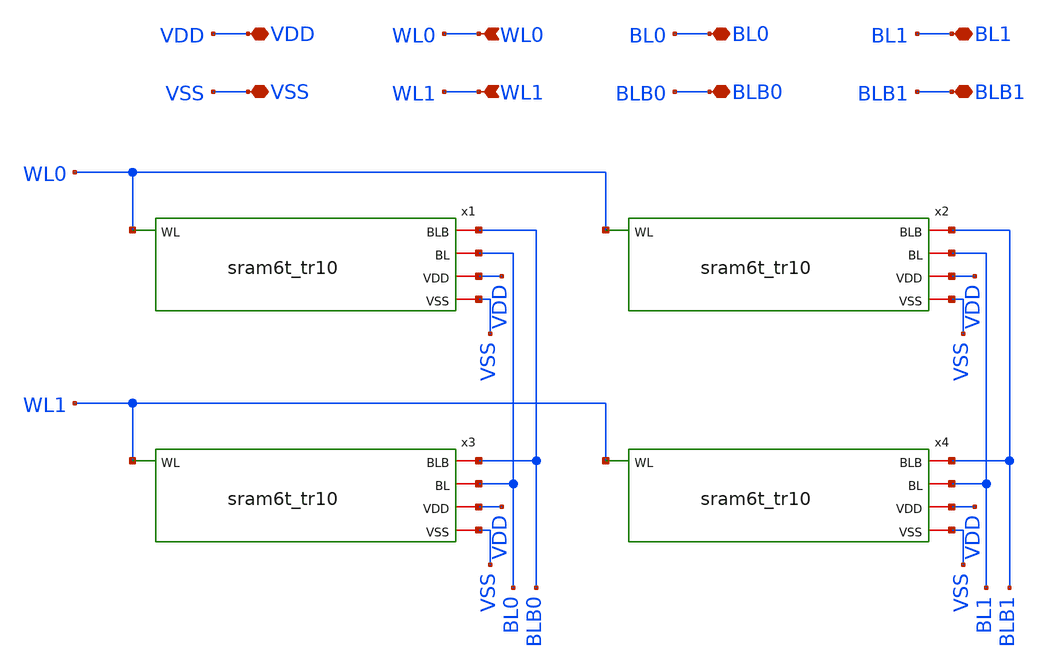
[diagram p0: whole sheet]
** sch_path: array/8word_x_2bit/sram_2w2b.sch
**.subckt sram_2w2b VDD VSS BL0 BLB0 BL1 BLB1 WL0 WL1
*.iopin VDD
*.iopin VSS
*.iopin BL0
*.iopin BLB0
*.iopin BL1
*.iopin BLB1
*.ipin WL0
*.ipin WL1
x1 BL0 BLB0 WL0 VDD VSS sram6t_tr10
x2 BL1 BLB1 WL0 VDD VSS sram6t_tr10
x3 BL0 BLB0 WL1 VDD VSS sram6t_tr10
x4 BL1 BLB1 WL1 VDD VSS sram6t_tr10
**.ends
.end
